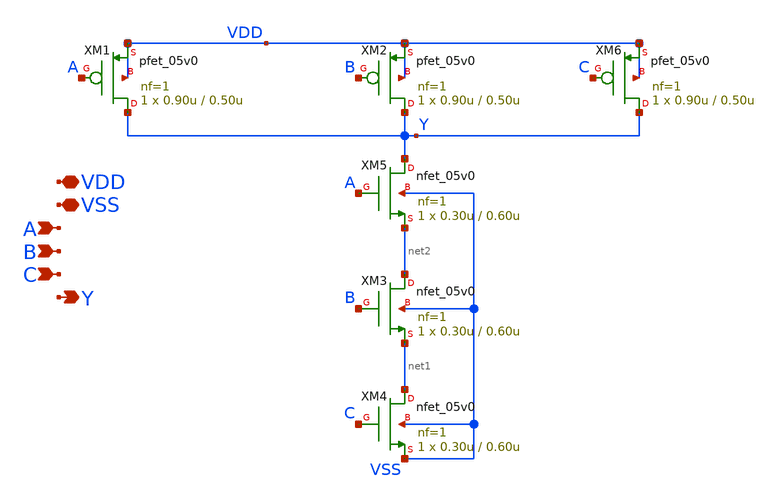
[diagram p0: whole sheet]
** sch_path: xschem/switch-matrix/nand3_1.sch
**.subckt nand3_1 VDD VSS A B Y C
*.iopin VDD
*.iopin VSS
*.ipin A
*.ipin B
*.opin Y
*.ipin C
XM1 Y A VDD VDD pfet_05v0 L=0.50u W=0.90u nf=1 ad='int((nf+1)/2) * W/nf * 0.18u' as='int((nf+2)/2) * W/nf * 0.18u'
+ pd='2*int((nf+1)/2) * (W/nf + 0.18u)' ps='2*int((nf+2)/2) * (W/nf + 0.18u)' nrd='0.18u / W' nrs='0.18u / W'
+ sa=0 sb=0 sd=0 m=1
XM2 Y B VDD VDD pfet_05v0 L=0.50u W=0.90u nf=1 ad='int((nf+1)/2) * W/nf * 0.18u' as='int((nf+2)/2) * W/nf * 0.18u'
+ pd='2*int((nf+1)/2) * (W/nf + 0.18u)' ps='2*int((nf+2)/2) * (W/nf + 0.18u)' nrd='0.18u / W' nrs='0.18u / W'
+ sa=0 sb=0 sd=0 m=1
XM3 net2 B net1 VSS nfet_05v0 L=0.60u W=0.30u nf=1 ad='int((nf+1)/2) * W/nf * 0.18u' as='int((nf+2)/2) * W/nf * 0.18u'
+ pd='2*int((nf+1)/2) * (W/nf + 0.18u)' ps='2*int((nf+2)/2) * (W/nf + 0.18u)' nrd='0.18u / W' nrs='0.18u / W'
+ sa=0 sb=0 sd=0 m=1
XM4 net1 C VSS VSS nfet_05v0 L=0.60u W=0.30u nf=1 ad='int((nf+1)/2) * W/nf * 0.18u' as='int((nf+2)/2) * W/nf * 0.18u'
+ pd='2*int((nf+1)/2) * (W/nf + 0.18u)' ps='2*int((nf+2)/2) * (W/nf + 0.18u)' nrd='0.18u / W' nrs='0.18u / W'
+ sa=0 sb=0 sd=0 m=1
XM5 Y A net2 VSS nfet_05v0 L=0.60u W=0.30u nf=1 ad='int((nf+1)/2) * W/nf * 0.18u' as='int((nf+2)/2) * W/nf * 0.18u'
+ pd='2*int((nf+1)/2) * (W/nf + 0.18u)' ps='2*int((nf+2)/2) * (W/nf + 0.18u)' nrd='0.18u / W' nrs='0.18u / W'
+ sa=0 sb=0 sd=0 m=1
XM6 Y C VDD VDD pfet_05v0 L=0.50u W=0.90u nf=1 ad='int((nf+1)/2) * W/nf * 0.18u' as='int((nf+2)/2) * W/nf * 0.18u'
+ pd='2*int((nf+1)/2) * (W/nf + 0.18u)' ps='2*int((nf+2)/2) * (W/nf + 0.18u)' nrd='0.18u / W' nrs='0.18u / W'
+ sa=0 sb=0 sd=0 m=1
**.ends
.end
